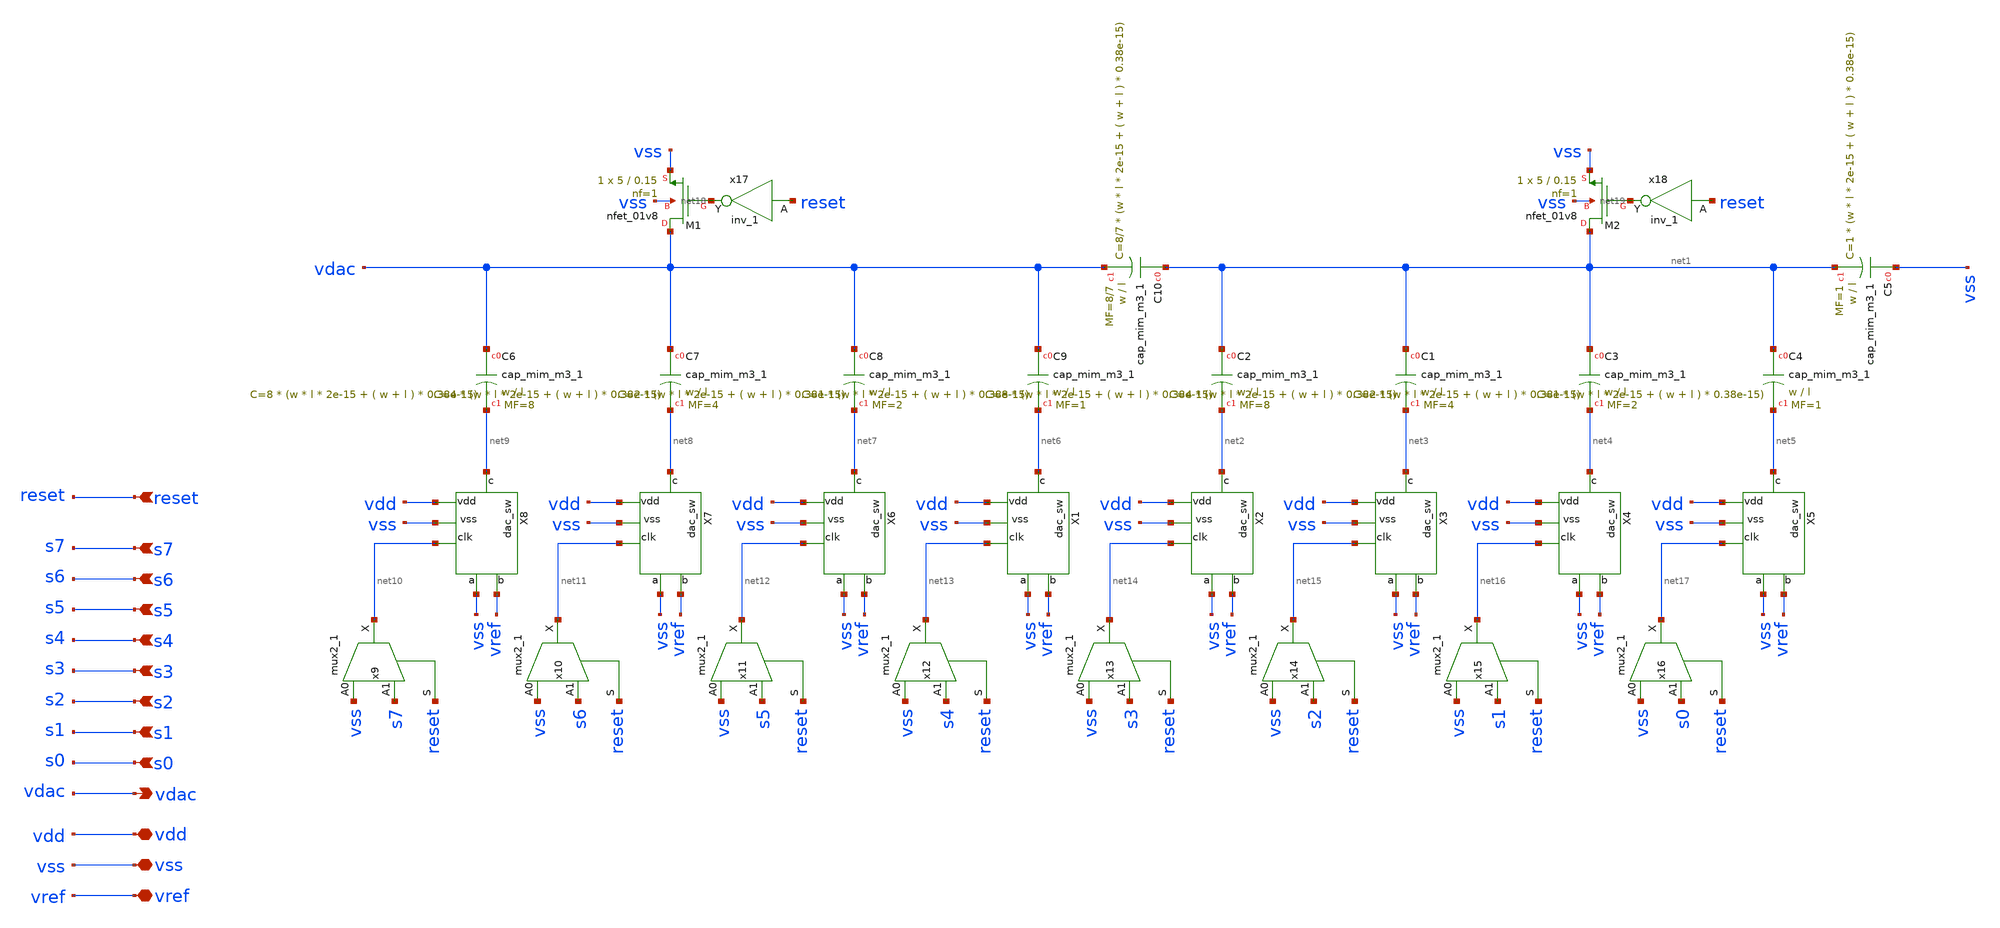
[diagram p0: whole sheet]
** sch_path: xschem/dac/dac.sch
**.subckt dac s7 s6 s5 s4 s3 s2 s1 s0 vdd vss vref vdac reset
*.ipin s7
*.ipin s6
*.ipin s5
*.ipin s4
*.ipin s3
*.ipin s2
*.ipin s1
*.ipin s0
*.iopin vdd
*.iopin vss
*.iopin vref
*.opin vdac
*.ipin reset
XC2 net1 net2 sky130_fd_pr__cap_mim_m3_1 W=w L=l MF=8 m=8
X2 net2 vref vss vdd net14 vss dac_sw
XC1 net1 net3 sky130_fd_pr__cap_mim_m3_1 W=w L=l MF=4 m=4
X3 net3 vref vss vdd net15 vss dac_sw
X4 net4 vref vss vdd net16 vss dac_sw
X5 net5 vref vss vdd net17 vss dac_sw
XC3 net1 net4 sky130_fd_pr__cap_mim_m3_1 W=w L=l MF=2 m=2
XC4 net1 net5 sky130_fd_pr__cap_mim_m3_1 W=w L=l MF=1 m=1
XC5 vss net1 sky130_fd_pr__cap_mim_m3_1 W=w L=l MF=1 m=1
X1 net6 vref vss vdd net13 vss dac_sw
X6 net7 vref vss vdd net12 vss dac_sw
X7 net8 vref vss vdd net11 vss dac_sw
X8 net9 vref vss vdd net10 vss dac_sw
x9 vss s7 reset vss vss vdd vdd net10 sky130_fd_sc_hd__mux2_1
x10 vss s6 reset vss vss vdd vdd net11 sky130_fd_sc_hd__mux2_1
x11 vss s5 reset vss vss vdd vdd net12 sky130_fd_sc_hd__mux2_1
x12 vss s4 reset vss vss vdd vdd net13 sky130_fd_sc_hd__mux2_1
x13 vss s3 reset vss vss vdd vdd net14 sky130_fd_sc_hd__mux2_1
x14 vss s2 reset vss vss vdd vdd net15 sky130_fd_sc_hd__mux2_1
x15 vss s1 reset vss vss vdd vdd net16 sky130_fd_sc_hd__mux2_1
x16 vss s0 reset vss vss vdd vdd net17 sky130_fd_sc_hd__mux2_1
XM1 vdac net18 vss vss sky130_fd_pr__nfet_01v8 L=0.15 W=5 nf=1 ad='int((nf+1)/2) * W/nf * 0.29' as='int((nf+2)/2) * W/nf * 0.29'
+ pd='2*int((nf+1)/2) * (W/nf + 0.29)' ps='2*int((nf+2)/2) * (W/nf + 0.29)' nrd='0.29 / W' nrs='0.29 / W'
+ sa=0 sb=0 sd=0 mult=1 m=1
x17 reset vss vss vdd vdd net18 sky130_fd_sc_hd__inv_1
XC10 net1 vdac sky130_fd_pr__cap_mim_m3_1 W=w L=l MF=8/7 m=8/7
XM2 net1 net19 vss vss sky130_fd_pr__nfet_01v8 L=0.15 W=5 nf=1 ad='int((nf+1)/2) * W/nf * 0.29' as='int((nf+2)/2) * W/nf * 0.29'
+ pd='2*int((nf+1)/2) * (W/nf + 0.29)' ps='2*int((nf+2)/2) * (W/nf + 0.29)' nrd='0.29 / W' nrs='0.29 / W'
+ sa=0 sb=0 sd=0 mult=1 m=1
x18 reset vss vss vdd vdd net19 sky130_fd_sc_hd__inv_1
XC6 vdac net9 sky130_fd_pr__cap_mim_m3_1 W=w L=l MF=8 m=8
XC7 vdac net8 sky130_fd_pr__cap_mim_m3_1 W=w L=l MF=4 m=4
XC8 vdac net7 sky130_fd_pr__cap_mim_m3_1 W=w L=l MF=2 m=2
XC9 vdac net6 sky130_fd_pr__cap_mim_m3_1 W=w L=l MF=1 m=1
**.ends

* expanding   symbol:  xschem/dac/dac_sw.sym # of pins=6
** sym_path: xschem/dac/dac_sw.sym
** sch_path: xschem/dac/dac_sw.sch
.subckt dac_sw c b vss vdd clk a
*.iopin vdd
*.iopin vss
*.ipin clk
*.iopin c
*.iopin a
*.iopin b
XM2 c clk b vss sky130_fd_pr__nfet_01v8 L=0.15 W=10 nf=1 ad='int((nf+1)/2) * W/nf * 0.29' as='int((nf+2)/2) * W/nf * 0.29'
+ pd='2*int((nf+1)/2) * (W/nf + 0.29)' ps='2*int((nf+2)/2) * (W/nf + 0.29)' nrd='0.29 / W' nrs='0.29 / W'
+ sa=0 sb=0 sd=0 mult=1 m=1
XM5 b net1 c vdd sky130_fd_pr__pfet_01v8 L=0.15 W=20 nf=1 ad='int((nf+1)/2) * W/nf * 0.29' as='int((nf+2)/2) * W/nf * 0.29'
+ pd='2*int((nf+1)/2) * (W/nf + 0.29)' ps='2*int((nf+2)/2) * (W/nf + 0.29)' nrd='0.29 / W' nrs='0.29 / W'
+ sa=0 sb=0 sd=0 mult=1 m=1
XM6 c net1 a vss sky130_fd_pr__nfet_01v8 L=0.15 W=10 nf=1 ad='int((nf+1)/2) * W/nf * 0.29' as='int((nf+2)/2) * W/nf * 0.29'
+ pd='2*int((nf+1)/2) * (W/nf + 0.29)' ps='2*int((nf+2)/2) * (W/nf + 0.29)' nrd='0.29 / W' nrs='0.29 / W'
+ sa=0 sb=0 sd=0 mult=1 m=1
XM7 a clk c vdd sky130_fd_pr__pfet_01v8 L=0.15 W=20 nf=1 ad='int((nf+1)/2) * W/nf * 0.29' as='int((nf+2)/2) * W/nf * 0.29'
+ pd='2*int((nf+1)/2) * (W/nf + 0.29)' ps='2*int((nf+2)/2) * (W/nf + 0.29)' nrd='0.29 / W' nrs='0.29 / W'
+ sa=0 sb=0 sd=0 mult=1 m=1
x1 clk vss vss vdd vdd net1 sky130_fd_sc_hd__inv_1
.ends

.end
